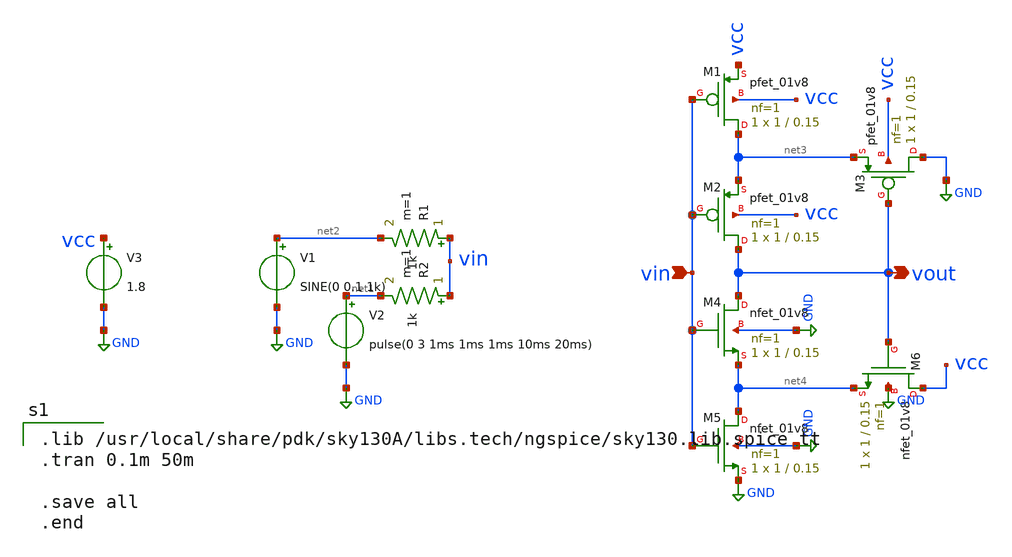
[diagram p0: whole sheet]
** sch_path: documents/CSTschematic.sch
**.subckt CSTschematic vin vout
*.ipin vin
*.opin vout
R1 vin net2 1k m=1
R2 vin net1 1k m=1
V1 net2 GND SINE(0 0.1 1k)
V2 net1 GND pulse(0 3 1ms 1ms 1ms 10ms 20ms)
XM1 net3 vin vcc vcc sky130_fd_pr__pfet_01v8 L=0.15 W=1 nf=1 ad='int((nf+1)/2) * W/nf * 0.29' as='int((nf+2)/2) * W/nf * 0.29'
+ pd='2*int((nf+1)/2) * (W/nf + 0.29)' ps='2*int((nf+2)/2) * (W/nf + 0.29)' nrd='0.29 / W' nrs='0.29 / W'
+ sa=0 sb=0 sd=0 mult=1 m=1
XM2 vout vin net3 vcc sky130_fd_pr__pfet_01v8 L=0.15 W=1 nf=1 ad='int((nf+1)/2) * W/nf * 0.29' as='int((nf+2)/2) * W/nf * 0.29'
+ pd='2*int((nf+1)/2) * (W/nf + 0.29)' ps='2*int((nf+2)/2) * (W/nf + 0.29)' nrd='0.29 / W' nrs='0.29 / W'
+ sa=0 sb=0 sd=0 mult=1 m=1
XM3 GND vout net3 vcc sky130_fd_pr__pfet_01v8 L=0.15 W=1 nf=1 ad='int((nf+1)/2) * W/nf * 0.29' as='int((nf+2)/2) * W/nf * 0.29'
+ pd='2*int((nf+1)/2) * (W/nf + 0.29)' ps='2*int((nf+2)/2) * (W/nf + 0.29)' nrd='0.29 / W' nrs='0.29 / W'
+ sa=0 sb=0 sd=0 mult=1 m=1
XM4 vout vin net4 GND sky130_fd_pr__nfet_01v8 L=0.15 W=1 nf=1 ad='int((nf+1)/2) * W/nf * 0.29' as='int((nf+2)/2) * W/nf * 0.29'
+ pd='2*int((nf+1)/2) * (W/nf + 0.29)' ps='2*int((nf+2)/2) * (W/nf + 0.29)' nrd='0.29 / W' nrs='0.29 / W'
+ sa=0 sb=0 sd=0 mult=1 m=1
XM5 net4 vin GND GND sky130_fd_pr__nfet_01v8 L=0.15 W=1 nf=1 ad='int((nf+1)/2) * W/nf * 0.29' as='int((nf+2)/2) * W/nf * 0.29'
+ pd='2*int((nf+1)/2) * (W/nf + 0.29)' ps='2*int((nf+2)/2) * (W/nf + 0.29)' nrd='0.29 / W' nrs='0.29 / W'
+ sa=0 sb=0 sd=0 mult=1 m=1
XM6 vcc vout net4 GND sky130_fd_pr__nfet_01v8 L=0.15 W=1 nf=1 ad='int((nf+1)/2) * W/nf * 0.29' as='int((nf+2)/2) * W/nf * 0.29'
+ pd='2*int((nf+1)/2) * (W/nf + 0.29)' ps='2*int((nf+2)/2) * (W/nf + 0.29)' nrd='0.29 / W' nrs='0.29 / W'
+ sa=0 sb=0 sd=0 mult=1 m=1
V3 vcc GND 1.8
**** begin user architecture code

.lib /usr/local/share/pdk/sky130A/libs.tech/ngspice/sky130.lib.spice tt
.tran 0.1m 50m

.save all
.end

**** end user architecture code
**.ends
.GLOBAL GND
.end
